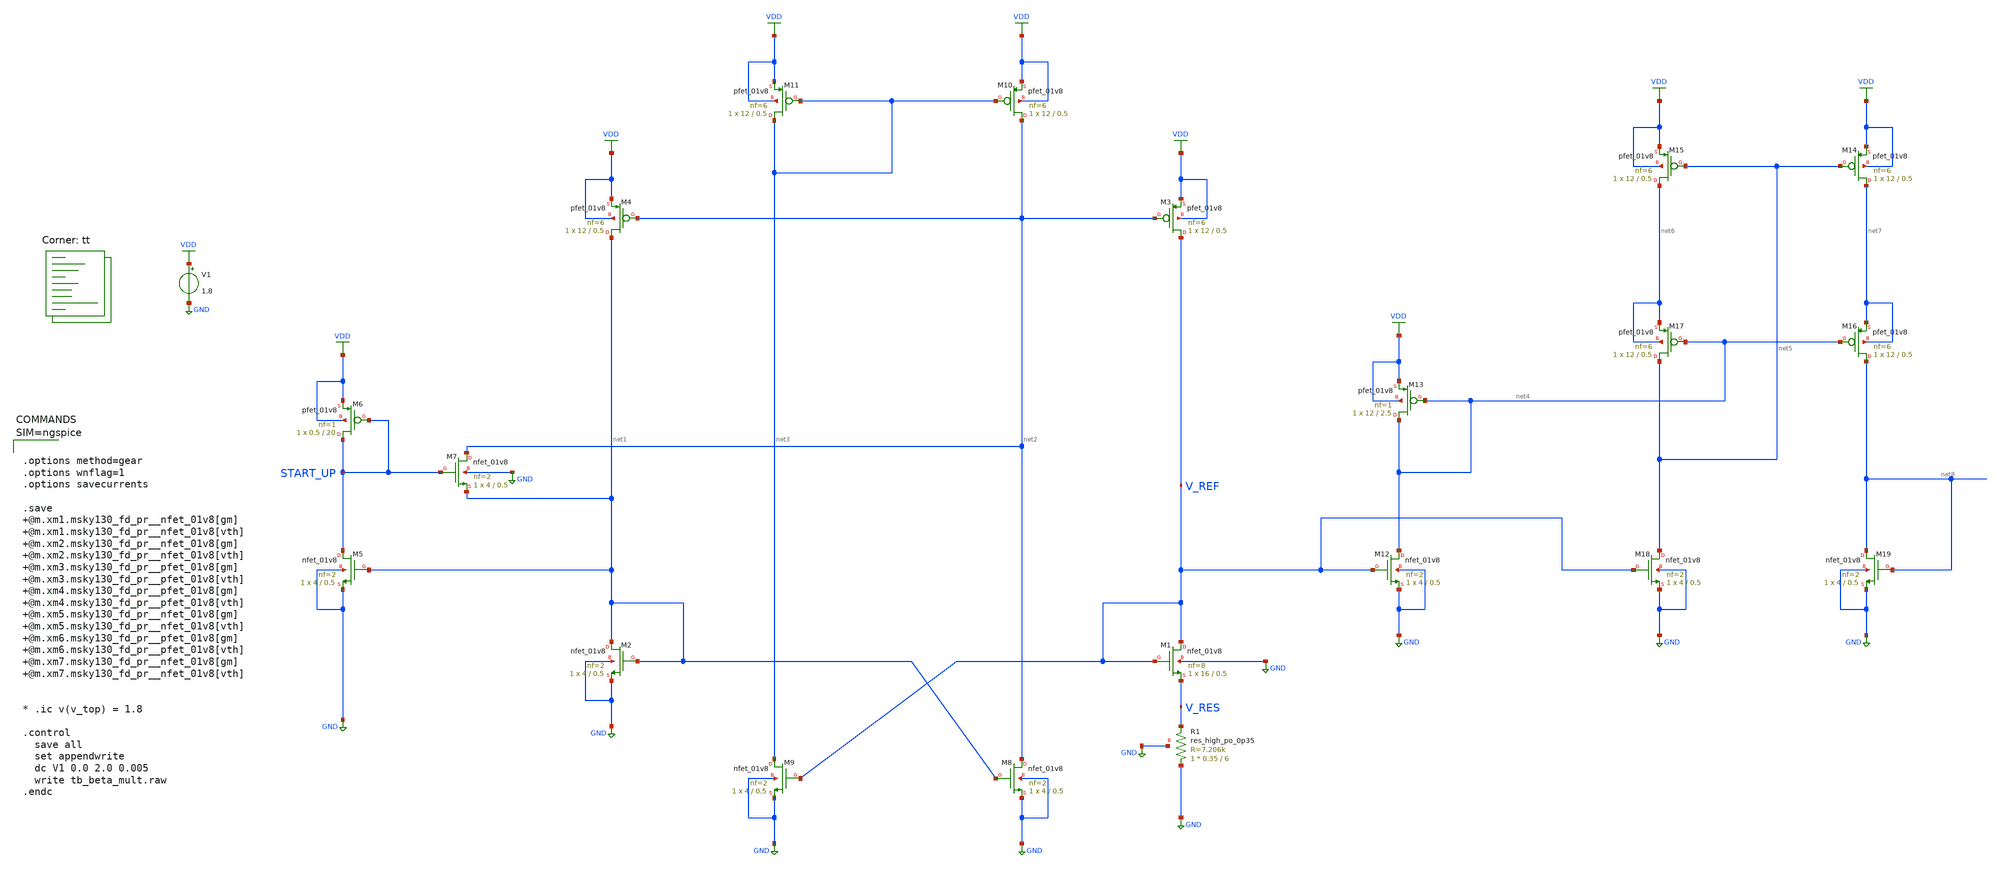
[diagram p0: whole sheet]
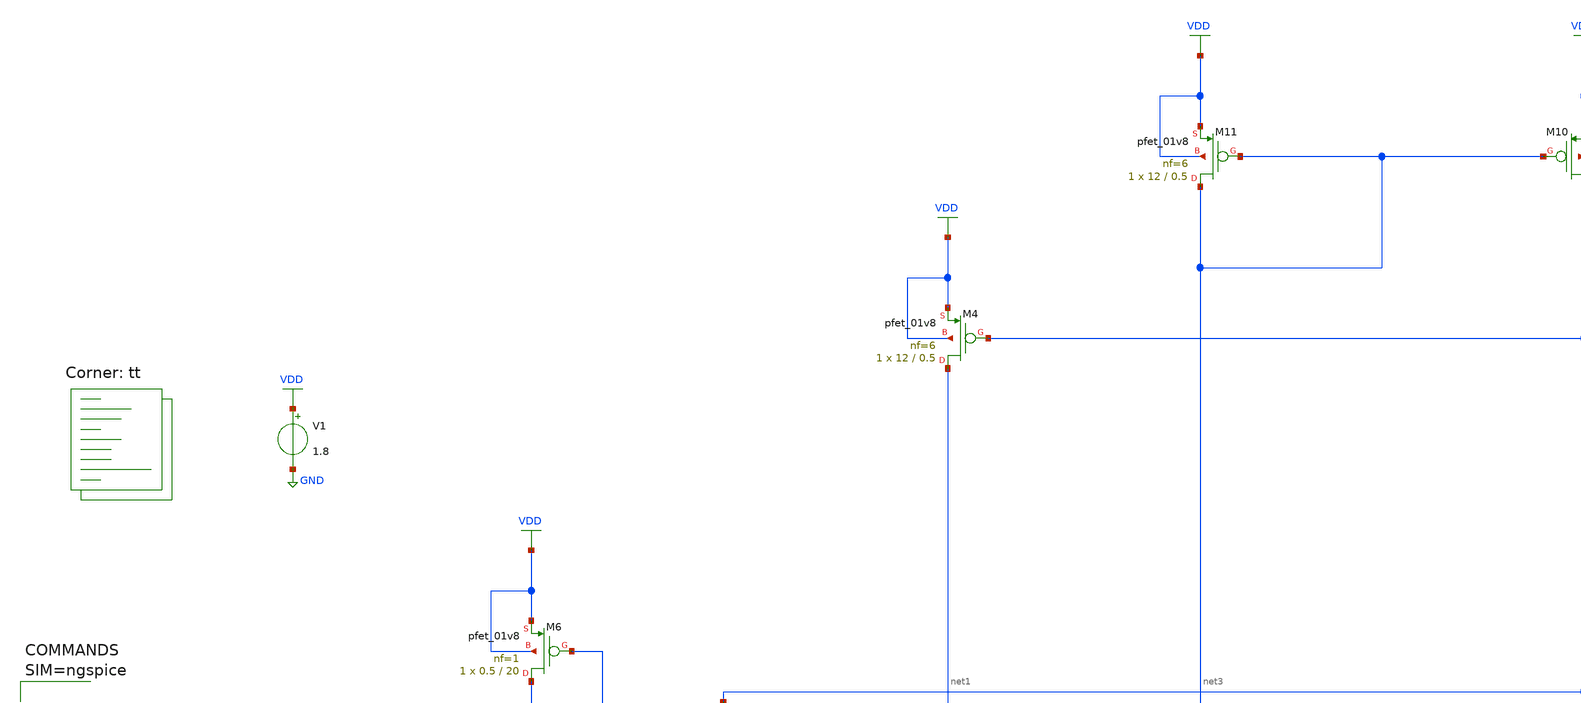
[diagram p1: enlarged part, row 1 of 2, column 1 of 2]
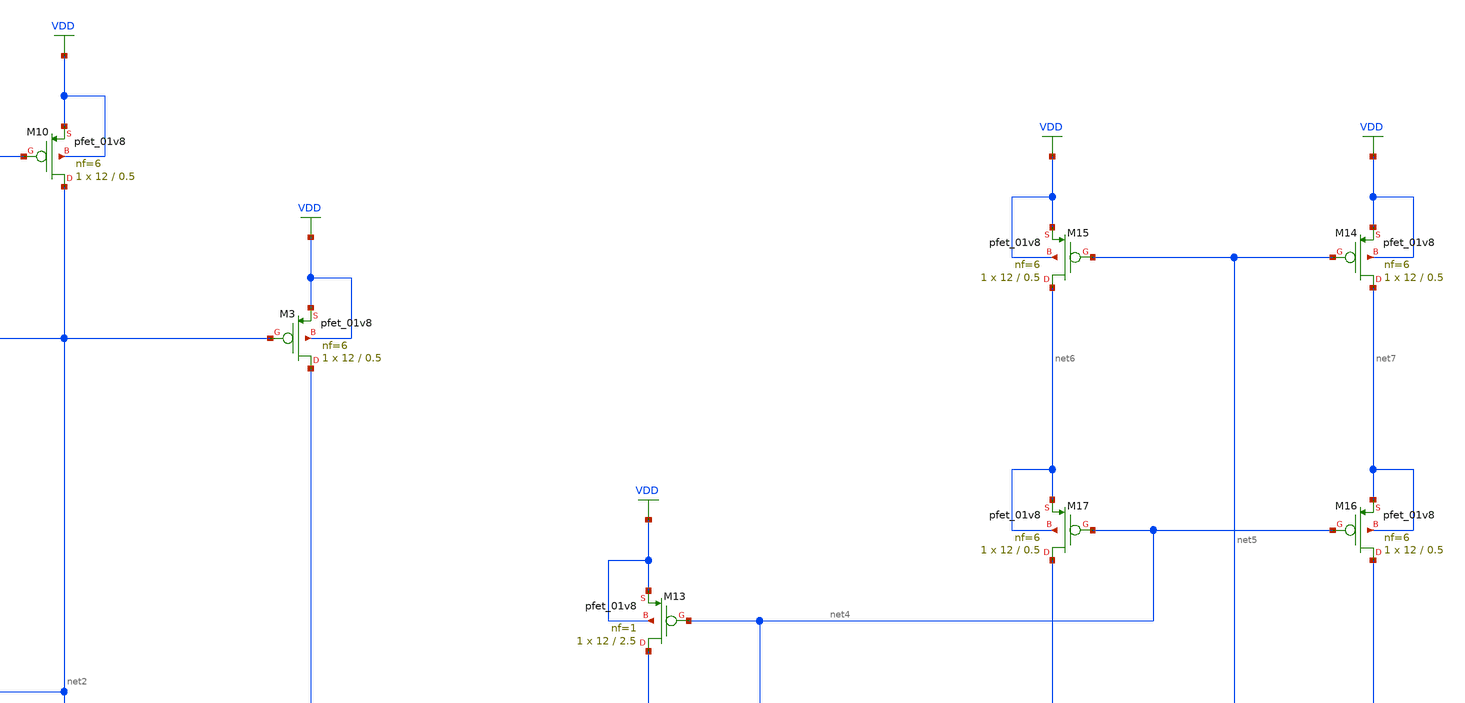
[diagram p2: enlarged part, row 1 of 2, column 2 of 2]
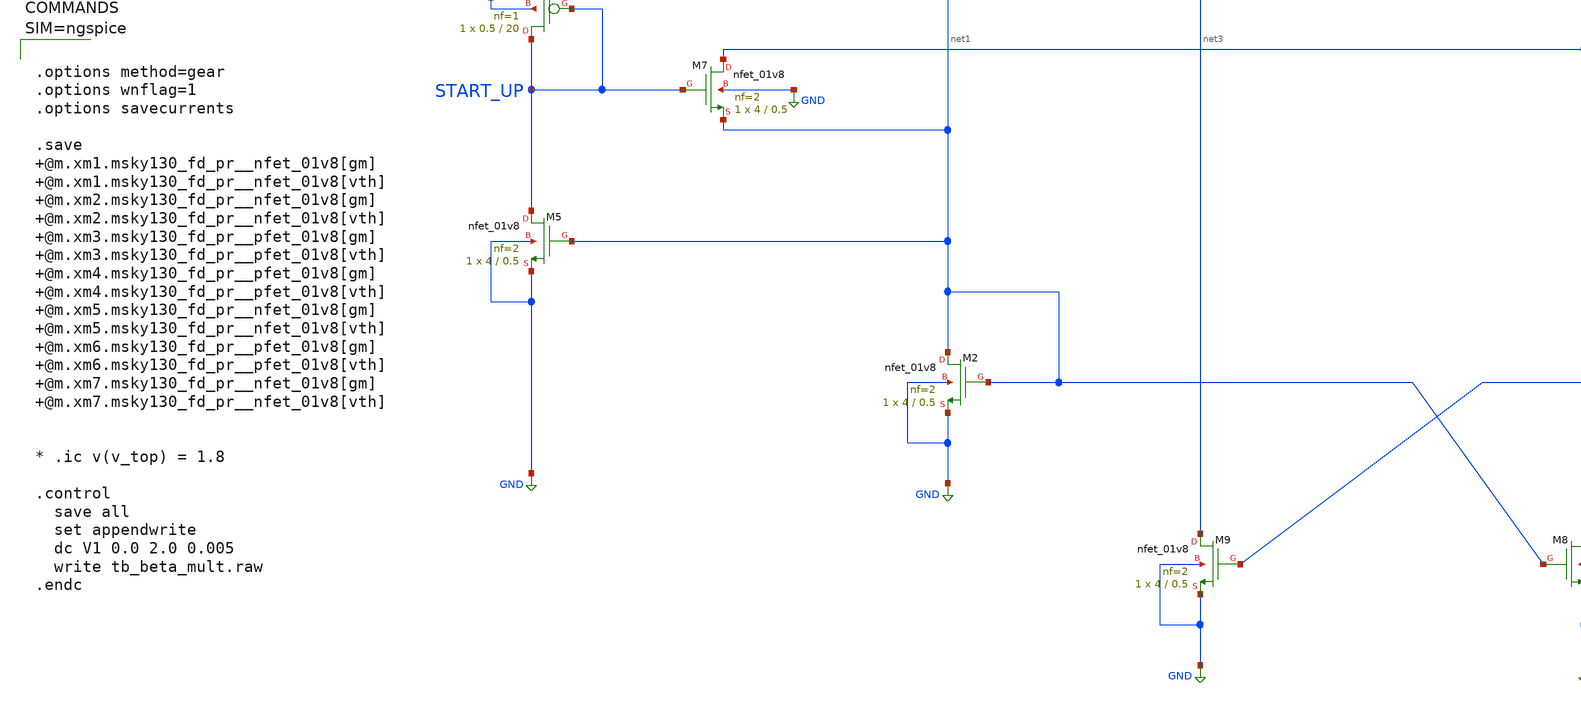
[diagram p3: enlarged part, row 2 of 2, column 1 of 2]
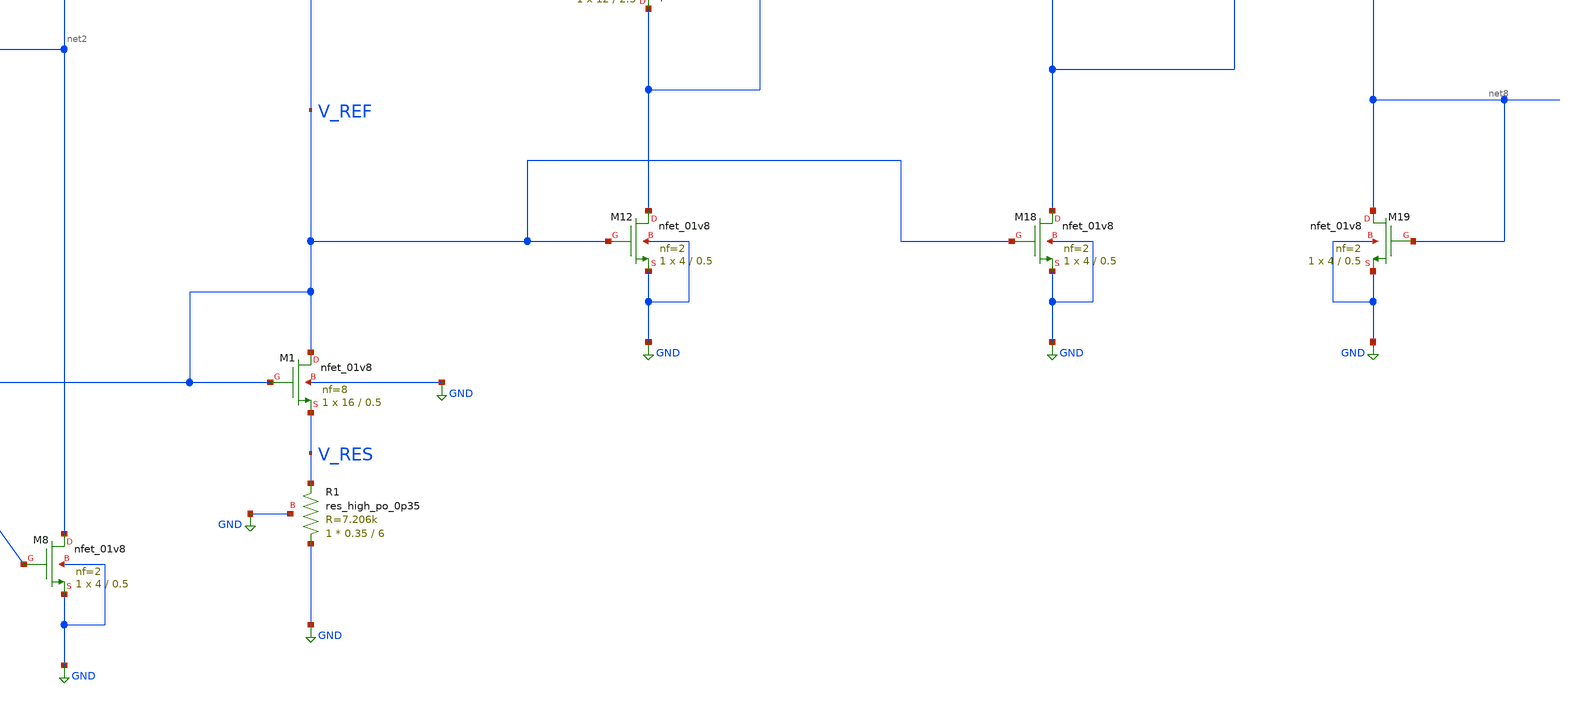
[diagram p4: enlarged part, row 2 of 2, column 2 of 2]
** sch_path: projects/ASU/EEE572/schematic/tb_beta_mult.sch
**.subckt tb_beta_mult
V1 VDD GND 1.8
XM1 V_REF V_REF V_RES GND sky130_fd_pr__nfet_01v8 L=0.5 W=16 nf=8 ad='int((nf+1)/2) * W/nf * 0.29' as='int((nf+2)/2) * W/nf * 0.29'
+ pd='2*int((nf+1)/2) * (W/nf + 0.29)' ps='2*int((nf+2)/2) * (W/nf + 0.29)' nrd='0.29 / W' nrs='0.29 / W'
+ sa=0 sb=0 sd=0 mult=1 m=1
XM2 net1 net1 GND GND sky130_fd_pr__nfet_01v8 L=0.5 W=4 nf=2 ad='int((nf+1)/2) * W/nf * 0.29' as='int((nf+2)/2) * W/nf * 0.29'
+ pd='2*int((nf+1)/2) * (W/nf + 0.29)' ps='2*int((nf+2)/2) * (W/nf + 0.29)' nrd='0.29 / W' nrs='0.29 / W'
+ sa=0 sb=0 sd=0 mult=1 m=1
XM5 START_UP net1 GND GND sky130_fd_pr__nfet_01v8 L=0.5 W=4 nf=2 ad='int((nf+1)/2) * W/nf * 0.29' as='int((nf+2)/2) * W/nf * 0.29'
+ pd='2*int((nf+1)/2) * (W/nf + 0.29)' ps='2*int((nf+2)/2) * (W/nf + 0.29)' nrd='0.29 / W' nrs='0.29 / W'
+ sa=0 sb=0 sd=0 mult=1 m=1
XM7 net2 START_UP net1 GND sky130_fd_pr__nfet_01v8 L=0.5 W=4 nf=2 ad='int((nf+1)/2) * W/nf * 0.29' as='int((nf+2)/2) * W/nf * 0.29'
+ pd='2*int((nf+1)/2) * (W/nf + 0.29)' ps='2*int((nf+2)/2) * (W/nf + 0.29)' nrd='0.29 / W' nrs='0.29 / W'
+ sa=0 sb=0 sd=0 mult=1 m=1
XR1 GND V_RES GND sky130_fd_pr__res_high_po_0p35 L=6 mult=1 m=1
XM6 START_UP START_UP VDD VDD sky130_fd_pr__pfet_01v8 L=20 W=0.5 nf=1 ad='int((nf+1)/2) * W/nf * 0.29'
+ as='int((nf+2)/2) * W/nf * 0.29' pd='2*int((nf+1)/2) * (W/nf + 0.29)' ps='2*int((nf+2)/2) * (W/nf + 0.29)'
+ nrd='0.29 / W' nrs='0.29 / W' sa=0 sb=0 sd=0 mult=1 m=1
XM3 V_REF net2 VDD VDD sky130_fd_pr__pfet_01v8 L=0.5 W=12 nf=6 ad='int((nf+1)/2) * W/nf * 0.29' as='int((nf+2)/2) * W/nf * 0.29'
+ pd='2*int((nf+1)/2) * (W/nf + 0.29)' ps='2*int((nf+2)/2) * (W/nf + 0.29)' nrd='0.29 / W' nrs='0.29 / W'
+ sa=0 sb=0 sd=0 mult=1 m=1
XM4 net1 net2 VDD VDD sky130_fd_pr__pfet_01v8 L=0.5 W=12 nf=6 ad='int((nf+1)/2) * W/nf * 0.29' as='int((nf+2)/2) * W/nf * 0.29'
+ pd='2*int((nf+1)/2) * (W/nf + 0.29)' ps='2*int((nf+2)/2) * (W/nf + 0.29)' nrd='0.29 / W' nrs='0.29 / W'
+ sa=0 sb=0 sd=0 mult=1 m=1
XM8 net2 net1 GND GND sky130_fd_pr__nfet_01v8 L=0.5 W=4 nf=2 ad='int((nf+1)/2) * W/nf * 0.29' as='int((nf+2)/2) * W/nf * 0.29'
+ pd='2*int((nf+1)/2) * (W/nf + 0.29)' ps='2*int((nf+2)/2) * (W/nf + 0.29)' nrd='0.29 / W' nrs='0.29 / W'
+ sa=0 sb=0 sd=0 mult=1 m=1
XM9 net3 V_REF GND GND sky130_fd_pr__nfet_01v8 L=0.5 W=4 nf=2 ad='int((nf+1)/2) * W/nf * 0.29' as='int((nf+2)/2) * W/nf * 0.29'
+ pd='2*int((nf+1)/2) * (W/nf + 0.29)' ps='2*int((nf+2)/2) * (W/nf + 0.29)' nrd='0.29 / W' nrs='0.29 / W'
+ sa=0 sb=0 sd=0 mult=1 m=1
XM10 net2 net3 VDD VDD sky130_fd_pr__pfet_01v8 L=0.5 W=12 nf=6 ad='int((nf+1)/2) * W/nf * 0.29' as='int((nf+2)/2) * W/nf * 0.29'
+ pd='2*int((nf+1)/2) * (W/nf + 0.29)' ps='2*int((nf+2)/2) * (W/nf + 0.29)' nrd='0.29 / W' nrs='0.29 / W'
+ sa=0 sb=0 sd=0 mult=1 m=1
XM11 net3 net3 VDD VDD sky130_fd_pr__pfet_01v8 L=0.5 W=12 nf=6 ad='int((nf+1)/2) * W/nf * 0.29' as='int((nf+2)/2) * W/nf * 0.29'
+ pd='2*int((nf+1)/2) * (W/nf + 0.29)' ps='2*int((nf+2)/2) * (W/nf + 0.29)' nrd='0.29 / W' nrs='0.29 / W'
+ sa=0 sb=0 sd=0 mult=1 m=1
XM12 net4 V_REF GND GND sky130_fd_pr__nfet_01v8 L=0.5 W=4 nf=2 ad='int((nf+1)/2) * W/nf * 0.29' as='int((nf+2)/2) * W/nf * 0.29'
+ pd='2*int((nf+1)/2) * (W/nf + 0.29)' ps='2*int((nf+2)/2) * (W/nf + 0.29)' nrd='0.29 / W' nrs='0.29 / W'
+ sa=0 sb=0 sd=0 mult=1 m=1
XM13 net4 net4 VDD VDD sky130_fd_pr__pfet_01v8 L=2.5 W=12 nf=1 ad='int((nf+1)/2) * W/nf * 0.29' as='int((nf+2)/2) * W/nf * 0.29'
+ pd='2*int((nf+1)/2) * (W/nf + 0.29)' ps='2*int((nf+2)/2) * (W/nf + 0.29)' nrd='0.29 / W' nrs='0.29 / W'
+ sa=0 sb=0 sd=0 mult=1 m=1
XM14 net7 net5 VDD VDD sky130_fd_pr__pfet_01v8 L=0.5 W=12 nf=6 ad='int((nf+1)/2) * W/nf * 0.29' as='int((nf+2)/2) * W/nf * 0.29'
+ pd='2*int((nf+1)/2) * (W/nf + 0.29)' ps='2*int((nf+2)/2) * (W/nf + 0.29)' nrd='0.29 / W' nrs='0.29 / W'
+ sa=0 sb=0 sd=0 mult=1 m=1
XM15 net6 net5 VDD VDD sky130_fd_pr__pfet_01v8 L=0.5 W=12 nf=6 ad='int((nf+1)/2) * W/nf * 0.29' as='int((nf+2)/2) * W/nf * 0.29'
+ pd='2*int((nf+1)/2) * (W/nf + 0.29)' ps='2*int((nf+2)/2) * (W/nf + 0.29)' nrd='0.29 / W' nrs='0.29 / W'
+ sa=0 sb=0 sd=0 mult=1 m=1
XM16 net8 net4 net7 net7 sky130_fd_pr__pfet_01v8 L=0.5 W=12 nf=6 ad='int((nf+1)/2) * W/nf * 0.29' as='int((nf+2)/2) * W/nf * 0.29'
+ pd='2*int((nf+1)/2) * (W/nf + 0.29)' ps='2*int((nf+2)/2) * (W/nf + 0.29)' nrd='0.29 / W' nrs='0.29 / W'
+ sa=0 sb=0 sd=0 mult=1 m=1
XM17 net5 net4 net6 net6 sky130_fd_pr__pfet_01v8 L=0.5 W=12 nf=6 ad='int((nf+1)/2) * W/nf * 0.29' as='int((nf+2)/2) * W/nf * 0.29'
+ pd='2*int((nf+1)/2) * (W/nf + 0.29)' ps='2*int((nf+2)/2) * (W/nf + 0.29)' nrd='0.29 / W' nrs='0.29 / W'
+ sa=0 sb=0 sd=0 mult=1 m=1
XM18 net5 V_REF GND GND sky130_fd_pr__nfet_01v8 L=0.5 W=4 nf=2 ad='int((nf+1)/2) * W/nf * 0.29' as='int((nf+2)/2) * W/nf * 0.29'
+ pd='2*int((nf+1)/2) * (W/nf + 0.29)' ps='2*int((nf+2)/2) * (W/nf + 0.29)' nrd='0.29 / W' nrs='0.29 / W'
+ sa=0 sb=0 sd=0 mult=1 m=1
XM19 net8 net8 GND GND sky130_fd_pr__nfet_01v8 L=0.5 W=4 nf=2 ad='int((nf+1)/2) * W/nf * 0.29' as='int((nf+2)/2) * W/nf * 0.29'
+ pd='2*int((nf+1)/2) * (W/nf + 0.29)' ps='2*int((nf+2)/2) * (W/nf + 0.29)' nrd='0.29 / W' nrs='0.29 / W'
+ sa=0 sb=0 sd=0 mult=1 m=1
**** begin user architecture code
.lib $::SKYWATER_MODELS/sky130.lib.spice tt



.options method=gear
.options wnflag=1
.options savecurrents

.save @m.xm1.msky130_fd_pr__nfet_01v8[gm] @m.xm1.msky130_fd_pr__nfet_01v8[vth] @m.xm2.msky130_fd_pr__nfet_01v8[gm] @m.xm2.msky130_fd_pr__nfet_01v8[vth] @m.xm3.msky130_fd_pr__pfet_01v8[gm] @m.xm3.msky130_fd_pr__pfet_01v8[vth] @m.xm4.msky130_fd_pr__pfet_01v8[gm] @m.xm4.msky130_fd_pr__pfet_01v8[vth] @m.xm5.msky130_fd_pr__nfet_01v8[gm] @m.xm5.msky130_fd_pr__nfet_01v8[vth] @m.xm6.msky130_fd_pr__pfet_01v8[gm] @m.xm6.msky130_fd_pr__pfet_01v8[vth] @m.xm7.msky130_fd_pr__nfet_01v8[gm] @m.xm7.msky130_fd_pr__nfet_01v8[vth]


* .ic v(v_top) = 1.8

.control
  save all
  set appendwrite
  dc V1 0.0 2.0 0.005
  write tb_beta_mult.raw
.endc





**** end user architecture code
**.ends
.GLOBAL GND
.GLOBAL VDD
.end
